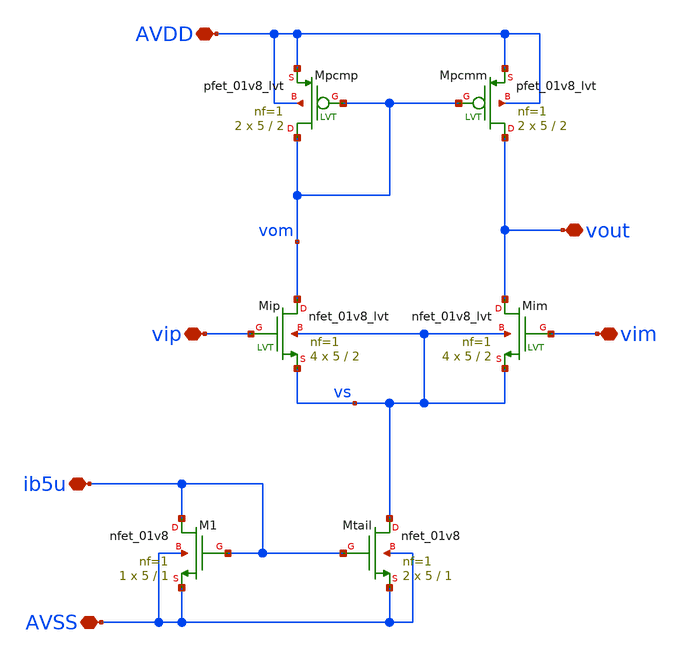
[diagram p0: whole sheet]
** sch_path: xschem/opa_nmos1.sch
**.subckt opa_nmos1 vip vim AVDD AVSS ib5u vout
*.iopin vip
*.iopin vim
*.iopin AVDD
*.iopin AVSS
*.iopin ib5u
*.iopin vout
XMtail vs ib5u AVSS AVSS sky130_fd_pr__nfet_01v8 L=1 W=5 nf=1 ad='int((1 + 1)/2) * 5 / 1 * 0.29' as='int((1 + 2)/2) * 5 / 1 * 0.29'
+ pd='2*int((1 + 1)/2) * (5 / 1 + 0.29)' ps='2*int((1 + 2)/2) * (5 / 1 + 0.29)' nrd='0.29 / 5 ' nrs='0.29 / 5 '
+ sa=0 sb=0 sd=0 mult=2 m=2
XM1 ib5u ib5u AVSS AVSS sky130_fd_pr__nfet_01v8 L=1 W=5 nf=1 ad='int((1 + 1)/2) * 5 / 1 * 0.29' as='int((1 + 2)/2) * 5 / 1 * 0.29'
+ pd='2*int((1 + 1)/2) * (5 / 1 + 0.29)' ps='2*int((1 + 2)/2) * (5 / 1 + 0.29)' nrd='0.29 / 5 ' nrs='0.29 / 5 '
+ sa=0 sb=0 sd=0 mult=1 m=1
XMip vom vip vs vs sky130_fd_pr__nfet_01v8_lvt L=2 W=5 nf=1 ad='int((1 + 1)/2) * 5 / 1 * 0.29' as='int((1 + 2)/2) * 5 / 1 * 0.29'
+ pd='2*int((1 + 1)/2) * (5 / 1 + 0.29)' ps='2*int((1 + 2)/2) * (5 / 1 + 0.29)' nrd='0.29 / 5 ' nrs='0.29 / 5 '
+ sa=0 sb=0 sd=0 mult=4 m=4
XMim vout vim vs vs sky130_fd_pr__nfet_01v8_lvt L=2 W=5 nf=1 ad='int((1 + 1)/2) * 5 / 1 * 0.29' as='int((1 + 2)/2) * 5 / 1 * 0.29'
+ pd='2*int((1 + 1)/2) * (5 / 1 + 0.29)' ps='2*int((1 + 2)/2) * (5 / 1 + 0.29)' nrd='0.29 / 5 ' nrs='0.29 / 5 '
+ sa=0 sb=0 sd=0 mult=4 m=4
XMpcmm vout vom AVDD AVDD sky130_fd_pr__pfet_01v8_lvt L=2 W=5 nf=1 ad='int((1 + 1)/2) * 5 / 1 * 0.29'
+ as='int((1 + 2)/2) * 5 / 1 * 0.29' pd='2*int((1 + 1)/2) * (5 / 1 + 0.29)' ps='2*int((1 + 2)/2) * (5 / 1 + 0.29)'
+ nrd='0.29 / 5 ' nrs='0.29 / 5 ' sa=0 sb=0 sd=0 mult=2 m=2
XMpcmp vom vom AVDD AVDD sky130_fd_pr__pfet_01v8_lvt L=2 W=5 nf=1 ad='int((1 + 1)/2) * 5 / 1 * 0.29'
+ as='int((1 + 2)/2) * 5 / 1 * 0.29' pd='2*int((1 + 1)/2) * (5 / 1 + 0.29)' ps='2*int((1 + 2)/2) * (5 / 1 + 0.29)'
+ nrd='0.29 / 5 ' nrs='0.29 / 5 ' sa=0 sb=0 sd=0 mult=2 m=2
**.ends
.end
